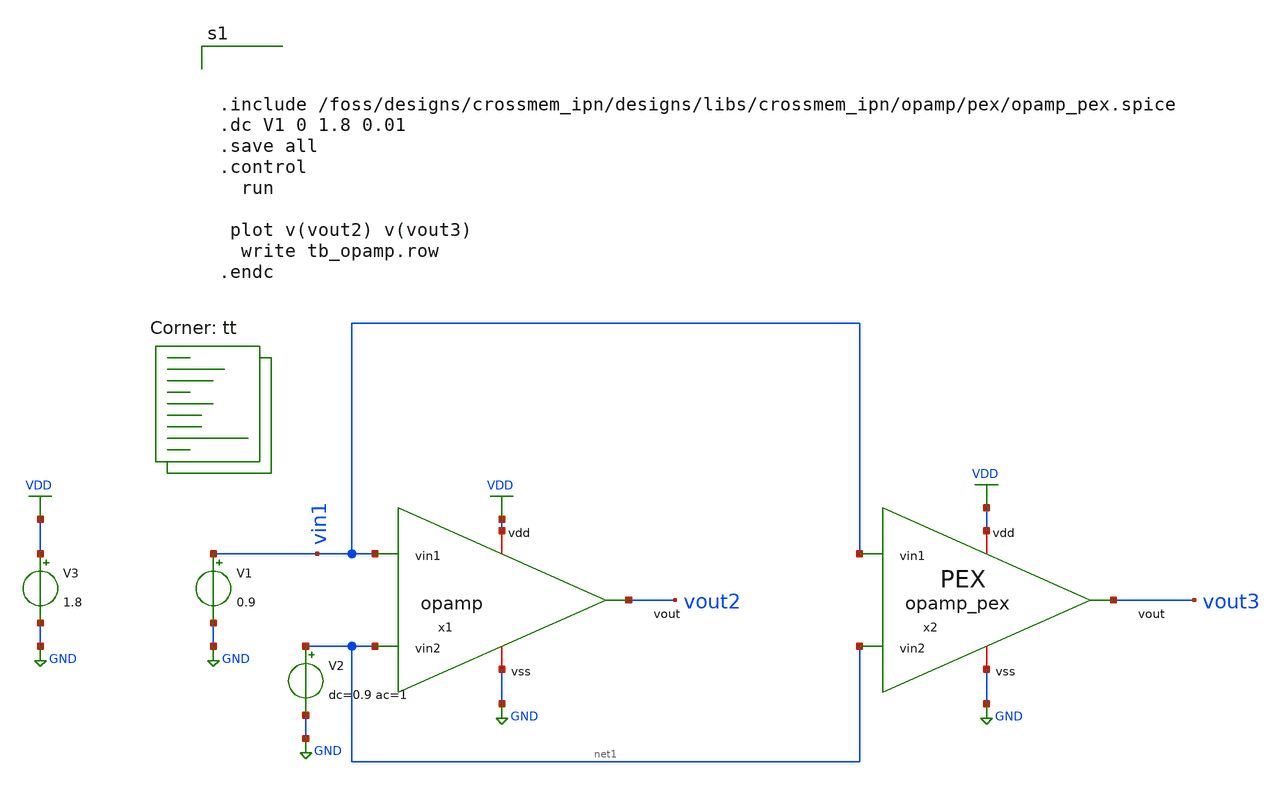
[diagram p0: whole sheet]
** sch_path: designs/libs/crossmem_ipn/opamp/tb_opamp.sch
**.subckt tb_opamp
x1 VDD vin1 net1 vout2 GND opamp
V3 VDD GND 1.8
V2 net1 GND dc=0.9 ac=1
V1 vin1 GND 0.9
x2 VDD GND vin1 net1 vout3 opamp_pex
**** begin user architecture code
.lib $::SKYWATER_MODELS/sky130.lib.spice tt



.include /foss/designs/crossmem_ipn/designs/libs/crossmem_ipn/opamp/pex/opamp_pex.spice
.dc V1 0 1.8 0.01
.save all
.control
  run

 plot v(vout2) v(vout3)
  write tb_opamp.row
.endc


**** end user architecture code
**.ends

* expanding   symbol:  opamp.sym # of pins=5
** sym_path: designs/libs/crossmem_ipn/opamp/opamp.sym
** sch_path: designs/libs/crossmem_ipn/opamp/opamp.sch
.subckt opamp vdd vin1 vin2 vout vss
*.iopin vss
*.iopin vdd
*.opin vout
*.ipin vin1
*.ipin vin2
XM3 net1 net1 vdd vdd sky130_fd_pr__pfet_01v8 L=1 W=9 nf=1 ad='int((1 + 1)/2) * 9 / 1 * 0.29' as='int((1 + 2)/2) * 9 / 1 * 0.29'
+ pd='2*int((1 + 1)/2) * (9 / 1 + 0.29)' ps='2*int((1 + 2)/2) * (9 / 1 + 0.29)' nrd='0.29 / 9 ' nrs='0.29 / 9 '
+ sa=0 sb=0 sd=0 mult=1 m=1
XM4 net2 net1 vdd vdd sky130_fd_pr__pfet_01v8 L=1 W=9 nf=1 ad='int((1 + 1)/2) * 9 / 1 * 0.29' as='int((1 + 2)/2) * 9 / 1 * 0.29'
+ pd='2*int((1 + 1)/2) * (9 / 1 + 0.29)' ps='2*int((1 + 2)/2) * (9 / 1 + 0.29)' nrd='0.29 / 9 ' nrs='0.29 / 9 '
+ sa=0 sb=0 sd=0 mult=1 m=1
XM6 vout net2 vdd vdd sky130_fd_pr__pfet_01v8 L=1 W=8.65 nf=20 ad='int((20 + 1)/2) * 8.65 / 20 * 0.29'
+ as='int((20 + 2)/2) * 8.65 / 20 * 0.29' pd='2*int((20 + 1)/2) * (8.65 / 20 + 0.29)' ps='2*int((20 + 2)/2) * (8.65 / 20 + 0.29)'
+ nrd='0.29 / 8.65 ' nrs='0.29 / 8.65 ' sa=0 sb=0 sd=0 mult=1 m=1
XM1 net1 vin1 net3 vss sky130_fd_pr__nfet_01v8 L=1 W=5 nf=1 ad='int((1 + 1)/2) * 5 / 1 * 0.29' as='int((1 + 2)/2) * 5 / 1 * 0.29'
+ pd='2*int((1 + 1)/2) * (5 / 1 + 0.29)' ps='2*int((1 + 2)/2) * (5 / 1 + 0.29)' nrd='0.29 / 5 ' nrs='0.29 / 5 '
+ sa=0 sb=0 sd=0 mult=1 m=1
XM2 net2 vin2 net3 vss sky130_fd_pr__nfet_01v8 L=1 W=5 nf=1 ad='int((1 + 1)/2) * 5 / 1 * 0.29' as='int((1 + 2)/2) * 5 / 1 * 0.29'
+ pd='2*int((1 + 1)/2) * (5 / 1 + 0.29)' ps='2*int((1 + 2)/2) * (5 / 1 + 0.29)' nrd='0.29 / 5 ' nrs='0.29 / 5 '
+ sa=0 sb=0 sd=0 mult=1 m=1
XM5 net3 vb1 vss vss sky130_fd_pr__nfet_01v8 L=1 W=8 nf=1 ad='int((1 + 1)/2) * 8 / 1 * 0.29' as='int((1 + 2)/2) * 8 / 1 * 0.29'
+ pd='2*int((1 + 1)/2) * (8 / 1 + 0.29)' ps='2*int((1 + 2)/2) * (8 / 1 + 0.29)' nrd='0.29 / 8 ' nrs='0.29 / 8 '
+ sa=0 sb=0 sd=0 mult=1 m=1
XM8 vb1 vb1 vss vss sky130_fd_pr__nfet_01v8 L=1 W=8 nf=1 ad='int((1 + 1)/2) * 8 / 1 * 0.29' as='int((1 + 2)/2) * 8 / 1 * 0.29'
+ pd='2*int((1 + 1)/2) * (8 / 1 + 0.29)' ps='2*int((1 + 2)/2) * (8 / 1 + 0.29)' nrd='0.29 / 8 ' nrs='0.29 / 8 '
+ sa=0 sb=0 sd=0 mult=1 m=1
XM7 vout vb1 vss vss sky130_fd_pr__nfet_01v8 L=1 W=7 nf=16 ad='int((16 + 1)/2) * 7 / 16 * 0.29' as='int((16 + 2)/2) * 7 / 16 * 0.29'
+ pd='2*int((16 + 1)/2) * (7 / 16 + 0.29)' ps='2*int((16 + 2)/2) * (7 / 16 + 0.29)' nrd='0.29 / 7 ' nrs='0.29 / 7 '
+ sa=0 sb=0 sd=0 mult=1 m=1
XC1 net2 vout sky130_fd_pr__cap_mim_m3_1 W=30 L=30 MF=1 m=1
XM9 vb1 vb1 vdd vdd sky130_fd_pr__pfet_01v8 L=0.5 W=0.5 nf=1 ad='int((1 + 1)/2) * 0.5 / 1 * 0.29' as='int((1 + 2)/2) * 0.5 / 1 * 0.29'
+ pd='2*int((1 + 1)/2) * (0.5 / 1 + 0.29)' ps='2*int((1 + 2)/2) * (0.5 / 1 + 0.29)' nrd='0.29 / 0.5 ' nrs='0.29 / 0.5 '
+ sa=0 sb=0 sd=0 mult=1 m=1
.ends

.GLOBAL GND
.GLOBAL VDD
.end
